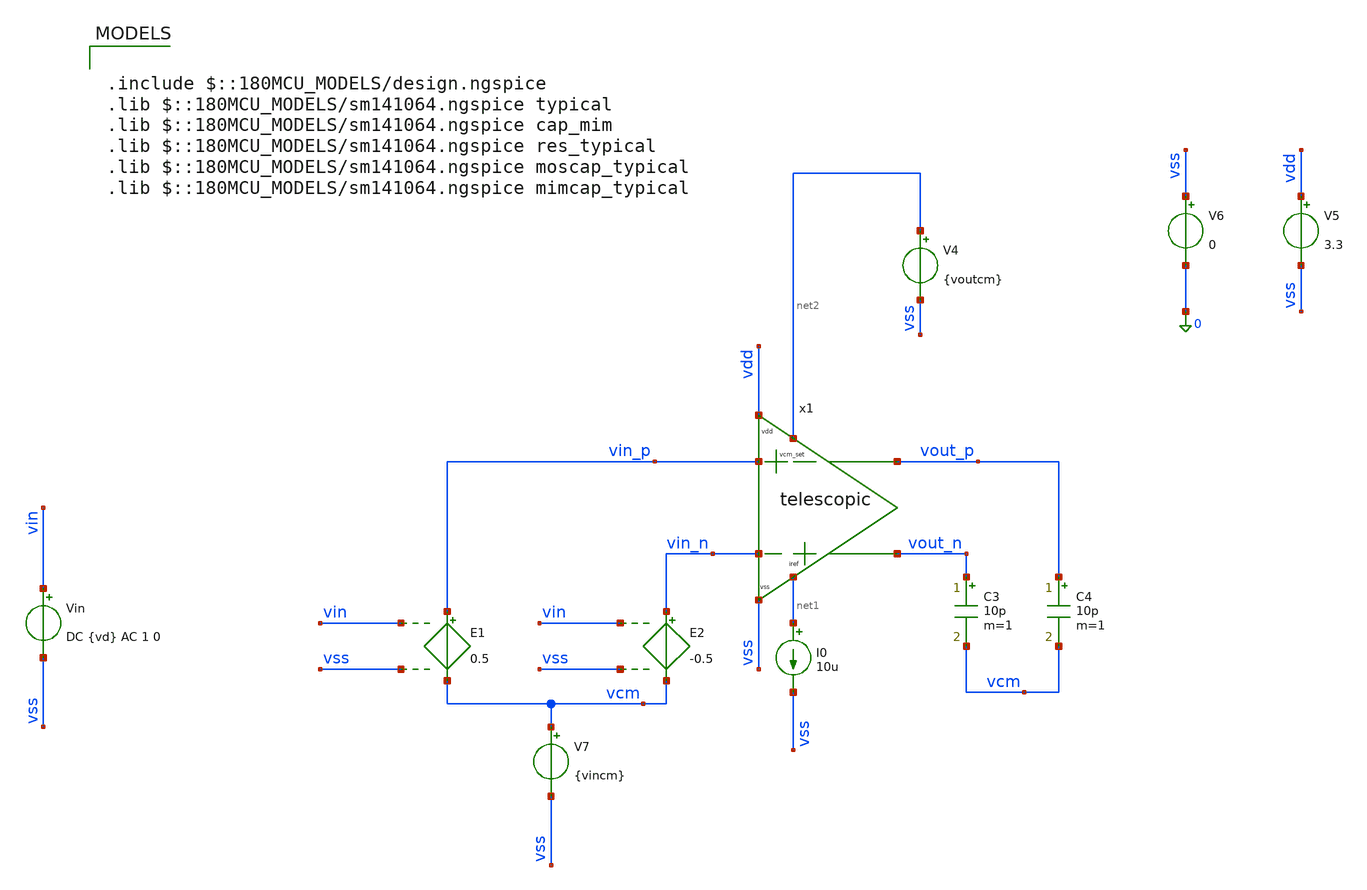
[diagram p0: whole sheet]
** sch_path: xschem/archive/rrl/telescopic_tb.sch
**.subckt telescopic_tb
I0 net1 vss 10u
V4 net2 vss {voutcm}
C3 vout_n vcm 10p m=1
C4 vout_p vcm 10p m=1
V5 vdd vss 3.3
V6 vss 0 0
V7 vcm vss {vincm}
E1 vin_p vcm vin vss 0.5
E2 vin_n vcm vin vss -0.5
Vin vin vss DC {vd} AC 1 0
x1 vin_p vin_n vout_n vout_p vdd vss net2 net1 telescopic
**** begin user architecture code

.param vincm=1
.param voutcm=0.8
.param vd=0
.control
save all
save @m.x1.x1.xm2.m0[id] @m.x1.x1.xm2.m0[gm] @m.x1.x1.xm2.m0[gds] @m.x1.x1.xm2.m0[cdb]
+ @m.x1.x1.xm2.m0[cgs] @m.x1.x1.xm2.m0[csb] @m.x1.x1.xm2.m0[cgd]
save @m.x1.x1.xm3.m0[id] @m.x1.x1.xm3.m0[gm] @m.x1.x1.xm3.m0[gds] @m.x1.x1.xm3.m0[cdb]
+ @m.x1.x1.xm3.m0[cgs] @m.x1.x1.xm3.m0[csb] @m.x1.x1.xm3.m0[cgd]
save @m.x1.x2.xm10.m0[id] @m.x1.x2.xm10.m0[gm] @m.x1.x2.xm10.m0[gds] @m.x1.x2.xm10.m0[cdb]
+ @m.x1.x2.xm10.m0[cgs] @m.x1.x2.xm10.m0[csb] @m.x1.x2.xm10.m0[cgd]
save @m.x1.x2.xm11.m0[id] @m.x1.x2.xm11.m0[gm] @m.x1.x2.xm11.m0[gds] @m.x1.x2.xm11.m0[cdb]
+ @m.x1.x2.xm11.m0[cgs] @m.x1.x2.xm11.m0[csb] @m.x1.x2.xm11.m0[cgd]
save @m.x1.x2.xm7.m0[id] @m.x1.x2.xm7.m0[gm] @m.x1.x2.xm7.m0[gds] @m.x1.x2.xm7.m0[cdb]
+ @m.x1.x2.xm7.m0[cgs] @m.x1.x2.xm7.m0[csb] @m.x1.x2.xm7.m0[cgd]
save @m.x1.x2.xm8.m0[id] @m.x1.x2.xm8.m0[gm] @m.x1.x2.xm8.m0[gds] @m.x1.x2.xm8.m0[cdb]
+ @m.x1.x2.xm8.m0[cgs] @m.x1.x2.xm8.m0[csb] @m.x1.x2.xm8.m0[cgd]
save @m.x1.x3.xm1.m0[id] @m.x1.x3.xm1.m0[gm] @m.x1.x3.xm1.m0[gds] @m.x1.x3.xm1.m0[cdb]
+ @m.x1.x3.xm1.m0[cgs] @m.x1.x3.xm1.m0[csb] @m.x1.x3.xm1.m0[cgd]
save @m.x1.x3.xm5.m0[id] @m.x1.x3.xm5.m0[gm] @m.x1.x3.xm5.m0[gds] @m.x1.x3.xm5.m0[cdb]
+ @m.x1.x3.xm5.m0[cgs] @m.x1.x3.xm5.m0[csb] @m.x1.x3.xm5.m0[cgd]
save @m.x1.x3.xm15.m0[id] @m.x1.x3.xm15.m0[gm] @m.x1.x3.xm15.m0[gds] @m.x1.x3.xm15.m0[cdb]
+ @m.x1.x3.xm15.m0[cgs] @m.x1.x3.xm15.m0[csb] @m.x1.x3.xm15.m0[cgd]
save @m.x1.x3.xm9.m0[id] @m.x1.x3.xm9.m0[gm] @m.x1.x3.xm9.m0[gds] @m.x1.x3.xm9.m0[cdb]
+ @m.x1.x3.xm9.m0[cgs] @m.x1.x3.xm9.m0[csb] @m.x1.x3.xm9.m0[cgd]
save @m.x1.x3.xm6.m0[id] @m.x1.x3.xm6.m0[gm] @m.x1.x3.xm6.m0[gds] @m.x1.x3.xm6.m0[cdb]
+ @m.x1.x3.xm6.m0[cgs] @m.x1.x3.xm6.m0[csb] @m.x1.x3.xm6.m0[cgd]
save @m.x1.x3.xm14.m0[id] @m.x1.x3.xm14.m0[gm] @m.x1.x3.xm14.m0[gds] @m.x1.x3.xm14.m0[cdb]
+ @m.x1.x3.xm14.m0[cgs] @m.x1.x3.xm14.m0[csb] @m.x1.x3.xm14.m0[cgd]
save @m.x1.x4.xm4.m0[id] @m.x1.x4.xm4.m0[gm] @m.x1.x4.xm4.m0[gds] @m.x1.x4.xm4.m0[cdb]
+ @m.x1.x4.xm4.m0[cgs] @m.x1.x4.xm4.m0[csb] @m.x1.x4.xm4.m0[cgd]
save @m.x1.x4.xm16.m0[id] @m.x1.x4.xm16.m0[gm] @m.x1.x4.xm16.m0[gds] @m.x1.x4.xm16.m0[cdb]
+ @m.x1.x4.xm16.m0[cgs] @m.x1.x4.xm16.m0[csb] @m.x1.x4.xm16.m0[cgd]
save @m.x1.x4.xm17.m0[id] @m.x1.x4.xm17.m0[gm] @m.x1.x4.xm17.m0[gds] @m.x1.x4.xm17.m0[cdb]
+ @m.x1.x4.xm17.m0[cgs] @m.x1.x4.xm17.m0[csb] @m.x1.x4.xm17.m0[cgd]
save @m.x1.x4.xm18.m0[id] @m.x1.x4.xm18.m0[gm] @m.x1.x4.xm18.m0[gds] @m.x1.x4.xm18.m0[cdb]
+ @m.x1.x4.xm18.m0[cgs] @m.x1.x4.xm18.m0[csb] @m.x1.x4.xm18.m0[cgd]
save @m.x1.x5.xm12.m0[id] @m.x1.x5.xm12.m0[gm] @m.x1.x5.xm12.m0[gds] @m.x1.x5.xm12.m0[cdb]
+ @m.x1.x5.xm12.m0[cgs] @m.x1.x5.xm12.m0[csb] @m.x1.x5.xm12.m0[cgd]
save @m.x1.x5.xm13.m0[id] @m.x1.x5.xm13.m0[gm] @m.x1.x5.xm13.m0[gds] @m.x1.x5.xm13.m0[cdb]
+ @m.x1.x5.xm13.m0[cgs] @m.x1.x5.xm13.m0[csb] @m.x1.x5.xm13.m0[cgd]
save @m.x1.x5.xm19.m0[id] @m.x1.x5.xm19.m0[gm] @m.x1.x5.xm19.m0[gds] @m.x1.x5.xm19.m0[cdb]
+ @m.x1.x5.xm19.m0[cgs] @m.x1.x5.xm19.m0[csb] @m.x1.x5.xm19.m0[cgd]
save @m.x1.x5.xm22.m0[id] @m.x1.x5.xm22.m0[gm] @m.x1.x5.xm22.m0[gds] @m.x1.x5.xm22.m0[cdb]
+ @m.x1.x5.xm22.m0[cgs] @m.x1.x5.xm22.m0[csb] @m.x1.x5.xm22.m0[cgd]
save @m.x1.x5.xm25.m0[id] @m.x1.x5.xm25.m0[gm] @m.x1.x5.xm25.m0[gds] @m.x1.x5.xm25.m0[cdb]
+ @m.x1.x5.xm25.m0[cgs] @m.x1.x5.xm25.m0[csb] @m.x1.x5.xm25.m0[cgd]
save @m.x1.x5.xm26.m0[id] @m.x1.x5.xm26.m0[gm] @m.x1.x5.xm26.m0[gds] @m.x1.x5.xm26.m0[cdb]
+ @m.x1.x5.xm26.m0[cgs] @m.x1.x5.xm26.m0[csb] @m.x1.x5.xm26.m0[cgd]
save @m.x1.x5.xm27.m0[id] @m.x1.x5.xm27.m0[gm] @m.x1.x5.xm27.m0[gds] @m.x1.x5.xm27.m0[cdb]
+ @m.x1.x5.xm27.m0[cgs] @m.x1.x5.xm27.m0[csb] @m.x1.x5.xm27.m0[cgd]
save @m.x1.x5.xm28.m0[id] @m.x1.x5.xm28.m0[gm] @m.x1.x5.xm28.m0[gds] @m.x1.x5.xm28.m0[cdb]
+ @m.x1.x5.xm28.m0[cgs] @m.x1.x5.xm28.m0[csb] @m.x1.x5.xm28.m0[cgd]
save @m.x1.x5.xm20.m0[id] @m.x1.x5.xm20.m0[gm] @m.x1.x5.xm20.m0[gds] @m.x1.x5.xm20.m0[cdb]
+ @m.x1.x5.xm20.m0[cgs] @m.x1.x5.xm20.m0[csb] @m.x1.x5.xm20.m0[cgd]
save @m.x1.x5.xm21.m0[id] @m.x1.x5.xm21.m0[gm] @m.x1.x5.xm21.m0[gds] @m.x1.x5.xm21.m0[cdb]
+ @m.x1.x5.xm21.m0[cgs] @m.x1.x5.xm21.m0[csb] @m.x1.x5.xm21.m0[cgd]
save @m.x1.x5.xm23.m0[id] @m.x1.x5.xm23.m0[gm] @m.x1.x5.xm23.m0[gds] @m.x1.x5.xm23.m0[cdb]
+ @m.x1.x5.xm23.m0[cgs] @m.x1.x5.xm23.m0[csb] @m.x1.x5.xm23.m0[cgd]

op
write ota_op.raw all
ac dec 100 1 10G
write ota_ac.raw all
*noise v(vout_p, vout_n) Vin dec 10 1 1000Meg
.endc



.include $::180MCU_MODELS/design.ngspice
.lib $::180MCU_MODELS/sm141064.ngspice typical
.lib $::180MCU_MODELS/sm141064.ngspice cap_mim
.lib $::180MCU_MODELS/sm141064.ngspice res_typical
.lib $::180MCU_MODELS/sm141064.ngspice moscap_typical
.lib $::180MCU_MODELS/sm141064.ngspice mimcap_typical

**** end user architecture code
**.ends
.end
